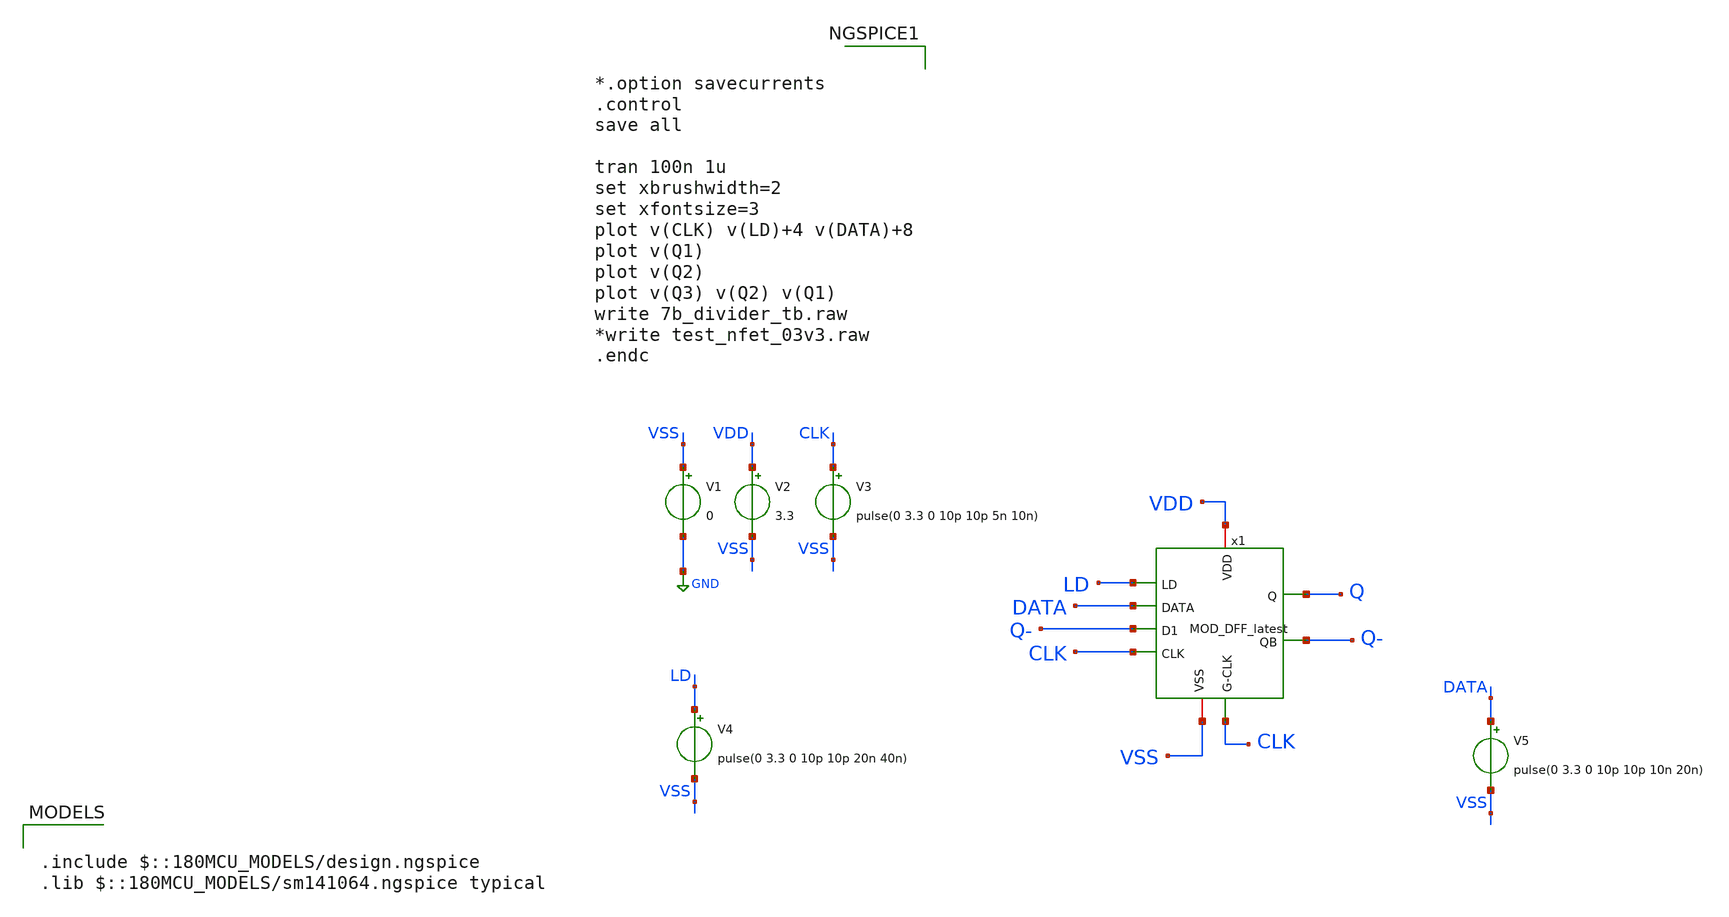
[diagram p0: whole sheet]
** sch_path: Clock_Generator_PAKISTAN_06/Schematics/untitled-17.sch
**.subckt untitled-17
x1 VDD LD DATA Q Q- Q- VSS CLK CLK MOD_DFF_latest
V1 VSS GND 0
V2 VDD VSS 3.3
V3 CLK VSS pulse(0 3.3 0 10p 10p 5n 10n)
V4 LD VSS pulse(0 3.3 0 10p 10p 20n 40n)
V5 DATA VSS pulse(0 3.3 0 10p 10p 10n 20n)
**** begin user architecture code


*.option savecurrents
.control
save all

tran 100n 1u
set xbrushwidth=2
set xfontsize=3
plot v(CLK) v(LD)+4 v(DATA)+8
plot v(Q1)
plot v(Q2)
plot v(Q3) v(Q2) v(Q1)
write 7b_divider_tb.raw
*write test_nfet_03v3.raw
.endc



.include $::180MCU_MODELS/design.ngspice
.lib $::180MCU_MODELS/sm141064.ngspice typical

**** end user architecture code
**.ends
.GLOBAL GND
.end
